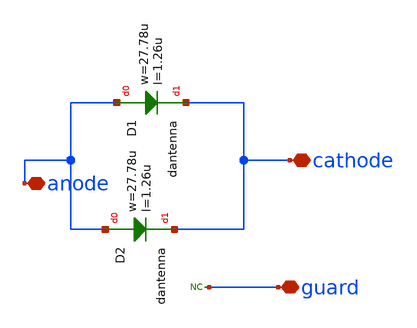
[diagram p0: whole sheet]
** sch_path: ihp-sg13g2/libs.ref/sg13g2_io/xschem/sg13g2_DCNDiode.sch
**.subckt sg13g2_DCNDiode cathode anode guard
*.iopin cathode
*.iopin anode
*.iopin guard
XD1 anode cathode dantenna l=1.26u w=27.78u
XD2 anode cathode dantenna l=1.26u w=27.78u
* noconn guard
**.ends
.end
